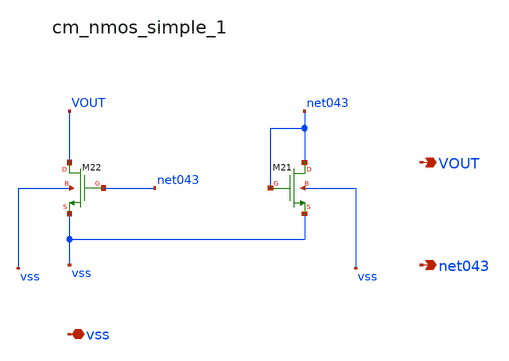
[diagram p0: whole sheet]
** sch_path: analog-db/raw/amp_002_alfio_raffc/hier/blocks/cm_nmos_simple_1.sch
**.subckt cm_nmos_simple_1 vss VOUT net043
*.iopin vss
*.opin VOUT
*.opin net043
XM21 net043 net043 vss vss sg13_lv_nmos w=x_dut_xm21_w l=x_dut_xm21_l ng=1 m=x_dut_xm21_m
XM22 VOUT net043 vss vss sg13_lv_nmos w=x_dut_xm22_w l=x_dut_xm22_l ng=1 m=x_dut_xm22_m
**.ends
.end
